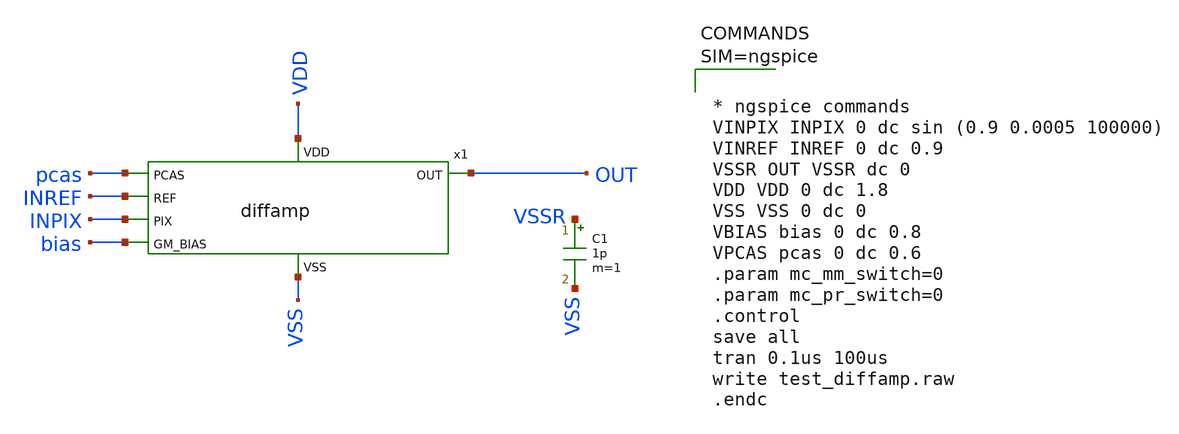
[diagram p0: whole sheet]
** sch_path: xschem/test_diffamp.sch
**.subckt test_diffamp
x1 pcas OUT INREF INPIX bias VDD VSS diffamp
C1 VSSR VSS 1p m=1
**** begin user architecture code

** opencircuitdesign pdks install
.lib $::SKYWATER_MODELS/sky130.lib.spice tt





* ngspice commands
VINPIX INPIX 0 dc sin (0.9 0.0005 100000)
VINREF INREF 0 dc 0.9
VSSR OUT VSSR dc 0
VDD VDD 0 dc 1.8
VSS VSS 0 dc 0
VBIAS bias 0 dc 0.8
VPCAS pcas 0 dc 0.6
.param mc_mm_switch=0
.param mc_pr_switch=0
.control
save all
tran 0.1us 100us
write test_diffamp.raw
.endc


**** end user architecture code
**.ends

* expanding   symbol:  diffamp/diffamp.sym # of pins=7
** sym_path: xschem/diffamp/diffamp.sym
** sch_path: xschem/diffamp/diffamp.sch
.subckt diffamp PCAS OUT REF PIX GM_BIAS VDD VSS
*.ipin PCAS
*.ipin PIX
*.ipin REF
*.ipin GM_BIAS
*.opin OUT
*.iopin VSS
*.iopin VDD
XM17 net4 GM_BIAS VSS VSS sky130_fd_pr__nfet_01v8_lvt L=15 W=20 nf=2 ad='int((2 + 1)/2) * 20 / 2 * 0.29'
+ as='int((2 + 2)/2) * 20 / 2 * 0.29' pd='2*int((2 + 1)/2) * (20 / 2 + 0.29)' ps='2*int((2 + 2)/2) * (20 / 2 + 0.29)'
+ nrd='0.29 / 20 ' nrs='0.29 / 20 ' sa=0 sb=0 sd=0 mult=1 m=1
XM8 net2 net1 VDD VDD sky130_fd_pr__pfet_01v8_lvt L=15 W=90 nf=3 ad='int((3 + 1)/2) * 90 / 3 * 0.29'
+ as='int((3 + 2)/2) * 90 / 3 * 0.29' pd='2*int((3 + 1)/2) * (90 / 3 + 0.29)' ps='2*int((3 + 2)/2) * (90 / 3 + 0.29)'
+ nrd='0.29 / 90 ' nrs='0.29 / 90 ' sa=0 sb=0 sd=0 mult=1 m=1
XM1 net3 net1 VDD VDD sky130_fd_pr__pfet_01v8_lvt L=15 W=90 nf=3 ad='int((3 + 1)/2) * 90 / 3 * 0.29'
+ as='int((3 + 2)/2) * 90 / 3 * 0.29' pd='2*int((3 + 1)/2) * (90 / 3 + 0.29)' ps='2*int((3 + 2)/2) * (90 / 3 + 0.29)'
+ nrd='0.29 / 90 ' nrs='0.29 / 90 ' sa=0 sb=0 sd=0 mult=1 m=1
XM2 OUT PCAS net2 VDD sky130_fd_pr__pfet_01v8_lvt L=3 W=90 nf=3 ad='int((3 + 1)/2) * 90 / 3 * 0.29' as='int((3 + 2)/2) * 90 / 3 * 0.29'
+ pd='2*int((3 + 1)/2) * (90 / 3 + 0.29)' ps='2*int((3 + 2)/2) * (90 / 3 + 0.29)' nrd='0.29 / 90 ' nrs='0.29 / 90 '
+ sa=0 sb=0 sd=0 mult=1 m=1
XM4 net1 PCAS net3 VDD sky130_fd_pr__pfet_01v8_lvt L=3 W=90 nf=3 ad='int((3 + 1)/2) * 90 / 3 * 0.29'
+ as='int((3 + 2)/2) * 90 / 3 * 0.29' pd='2*int((3 + 1)/2) * (90 / 3 + 0.29)' ps='2*int((3 + 2)/2) * (90 / 3 + 0.29)'
+ nrd='0.29 / 90 ' nrs='0.29 / 90 ' sa=0 sb=0 sd=0 mult=1 m=1
XM5 OUT PIX net4 VSS sky130_fd_pr__nfet_01v8_lvt L=3.5 W=800 nf=35 ad='int((35 + 1)/2) * 800 / 35 * 0.29'
+ as='int((35 + 2)/2) * 800 / 35 * 0.29' pd='2*int((35 + 1)/2) * (800 / 35 + 0.29)' ps='2*int((35 + 2)/2) * (800 / 35 + 0.29)'
+ nrd='0.29 / 800 ' nrs='0.29 / 800 ' sa=0 sb=0 sd=0 mult=1 m=1
XM6 net1 REF net4 VSS sky130_fd_pr__nfet_01v8_lvt L=3.5 W=800 nf=35 ad='int((35 + 1)/2) * 800 / 35 * 0.29'
+ as='int((35 + 2)/2) * 800 / 35 * 0.29' pd='2*int((35 + 1)/2) * (800 / 35 + 0.29)' ps='2*int((35 + 2)/2) * (800 / 35 + 0.29)'
+ nrd='0.29 / 800 ' nrs='0.29 / 800 ' sa=0 sb=0 sd=0 mult=1 m=1
.ends

.end
